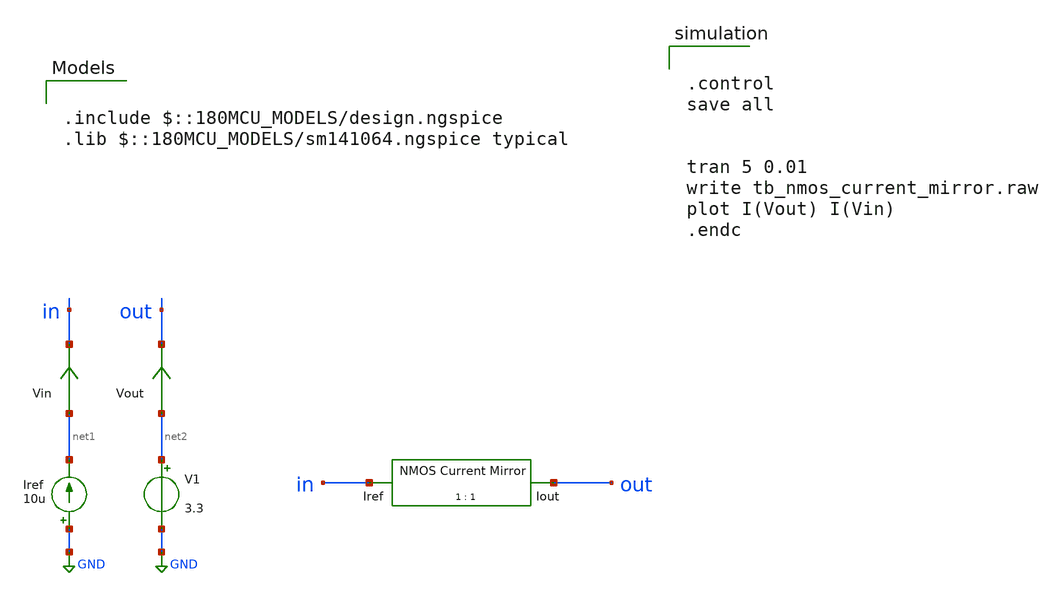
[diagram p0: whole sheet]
** sch_path: designs/libs/tb_analog/tb_nmos_current_mirror/tb_nmos_current_mirror.sch
**.subckt tb_nmos_current_mirror
Iref GND net1 10u
V1 net2 GND 3.3
Vin net1 in 0
.save i(vin)
Vout net2 out 0
.save i(vout)
x1 in out nmos_current_mirror
**** begin user architecture code


.control
save all


tran 5 0.01
write tb_nmos_current_mirror.raw
plot I(Vout) I(Vin)
.endc



.include $::180MCU_MODELS/design.ngspice
.lib $::180MCU_MODELS/sm141064.ngspice typical

**** end user architecture code
**.ends

* expanding   symbol:  libs/core_analog/current-mirror/nmos_current_mirror.sym # of pins=2
** sym_path: designs/libs/core_analog/current-mirror/nmos_current_mirror.sym
** sch_path: designs/libs/core_analog/current-mirror/nmos_current_mirror.sch
.subckt nmos_current_mirror Iref Iout
*.ipin Iref
*.opin Iout
XM1 Iref Iref net1 net1 nfet_03v3 L=0.28u W=0.22u nf=1 ad='int((nf+1)/2) * W/nf * 0.18u' as='int((nf+2)/2) * W/nf * 0.18u'
+ pd='2*int((nf+1)/2) * (W/nf + 0.18u)' ps='2*int((nf+2)/2) * (W/nf + 0.18u)' nrd='0.18u / W' nrs='0.18u / W'
+ sa=0 sb=0 sd=0 m=1
XM2 Iout Iref net2 net2 nfet_03v3 L=0.28u W=0.22u nf=1 ad='int((nf+1)/2) * W/nf * 0.18u' as='int((nf+2)/2) * W/nf * 0.18u'
+ pd='2*int((nf+1)/2) * (W/nf + 0.18u)' ps='2*int((nf+2)/2) * (W/nf + 0.18u)' nrd='0.18u / W' nrs='0.18u / W'
+ sa=0 sb=0 sd=0 m=1
XM3 net1 net1 GND GND nfet_03v3 L=0.28u W=0.22u nf=1 ad='int((nf+1)/2) * W/nf * 0.18u' as='int((nf+2)/2) * W/nf * 0.18u'
+ pd='2*int((nf+1)/2) * (W/nf + 0.18u)' ps='2*int((nf+2)/2) * (W/nf + 0.18u)' nrd='0.18u / W' nrs='0.18u / W'
+ sa=0 sb=0 sd=0 m=1
XM4 net2 net1 GND GND nfet_03v3 L=0.28u W=0.22u nf=1 ad='int((nf+1)/2) * W/nf * 0.18u' as='int((nf+2)/2) * W/nf * 0.18u'
+ pd='2*int((nf+1)/2) * (W/nf + 0.18u)' ps='2*int((nf+2)/2) * (W/nf + 0.18u)' nrd='0.18u / W' nrs='0.18u / W'
+ sa=0 sb=0 sd=0 m=1
.ends

.GLOBAL GND
.end
